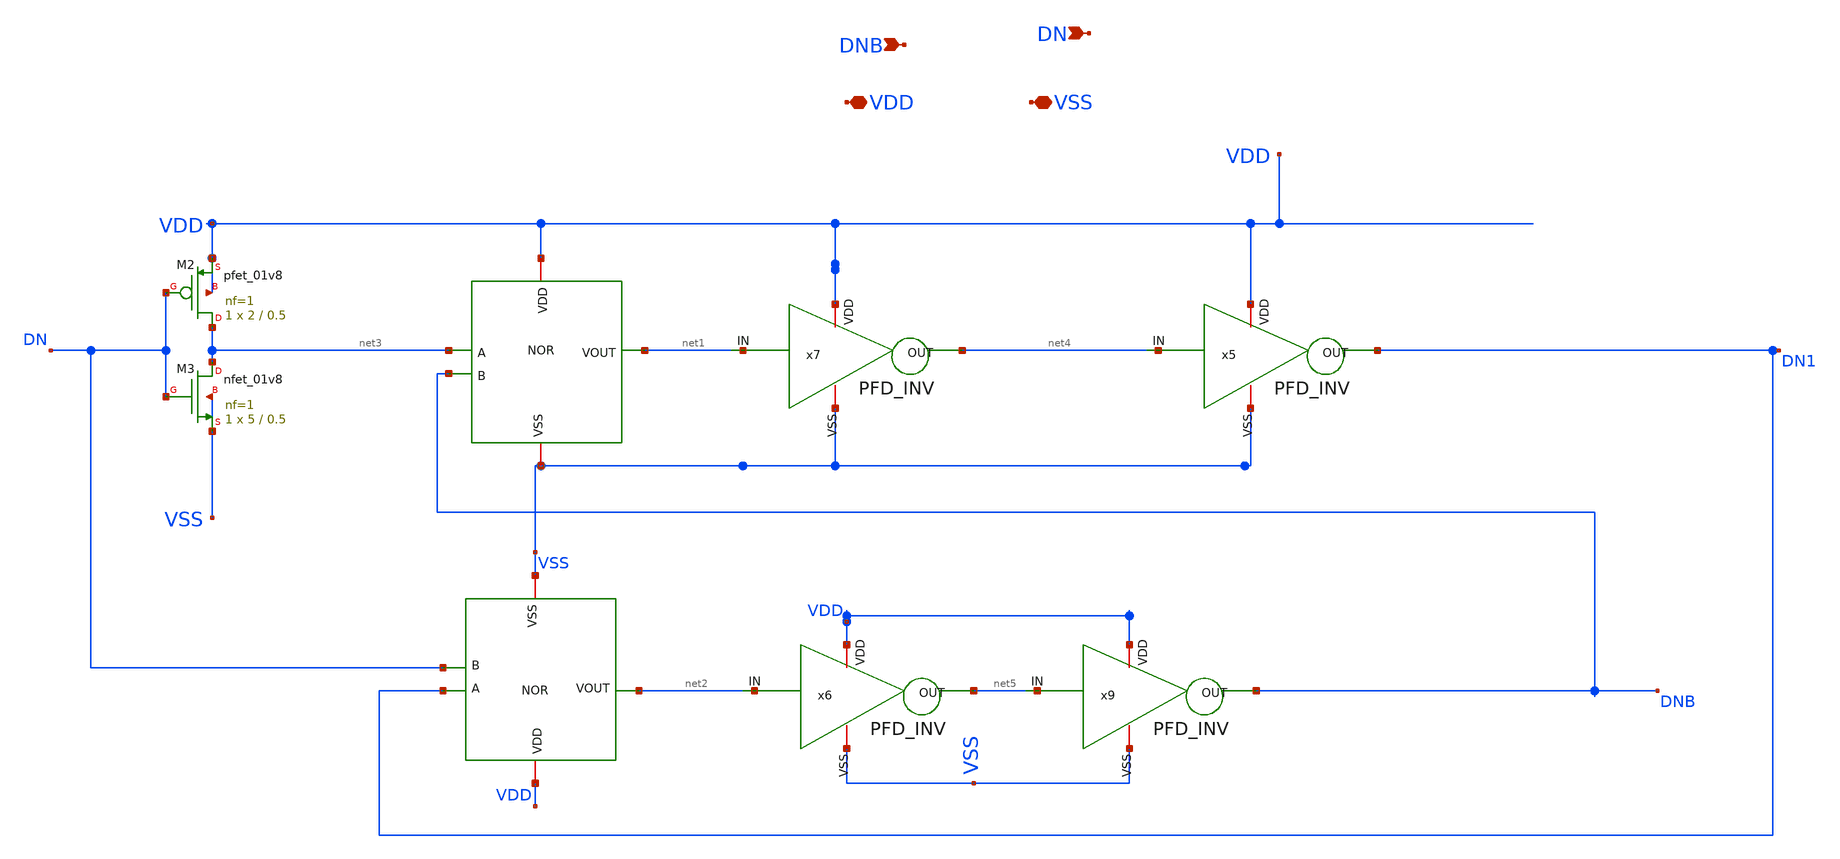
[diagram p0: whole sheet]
** sch_path: Xschem/PLL_TOP_Schematics/untitled.sch
**.subckt untitled DN DNB VDD VSS
*.ipin DN
*.ipin DNB
*.iopin VDD
*.iopin VSS
x3 VDD net3 DNB net1 VSS NOR
x4 VDD DN1 DN net2 VSS NOR
x6 VDD VSS net2 net5 PFD_INV
x7 VDD VSS net1 net4 PFD_INV
XM2 net3 DN VDD VDD sky130_fd_pr__pfet_01v8 L=0.5 W=2 nf=1 ad='int((nf+1)/2) * W/nf * 0.29' as='int((nf+2)/2) * W/nf * 0.29'
+ pd='2*int((nf+1)/2) * (W/nf + 0.29)' ps='2*int((nf+2)/2) * (W/nf + 0.29)' nrd='0.29 / W' nrs='0.29 / W'
+ sa=0 sb=0 sd=0 mult=1 m=1
XM3 net3 DN VSS VSS sky130_fd_pr__nfet_01v8 L=0.5 W=5 nf=1 ad='int((nf+1)/2) * W/nf * 0.29' as='int((nf+2)/2) * W/nf * 0.29'
+ pd='2*int((nf+1)/2) * (W/nf + 0.29)' ps='2*int((nf+2)/2) * (W/nf + 0.29)' nrd='0.29 / W' nrs='0.29 / W'
+ sa=0 sb=0 sd=0 mult=1 m=1
x5 VDD VSS net4 DN1 PFD_INV
x9 VDD VSS net5 DNB PFD_INV
**.ends

* expanding   symbol:  NOR.sym # of pins=5
** sym_path: Xschem/PLL_TOP_Schematics/NOR.sym
** sch_path: Xschem/PLL_TOP_Schematics/NOR.sch
.subckt NOR VDD A B VOUT VSS
*.iopin VSS
*.iopin VDD
*.ipin A
*.ipin B
*.opin VOUT
XM5 VOUT B net1 VDD sky130_fd_pr__pfet_01v8 L=0.2 W=4 nf=1 ad='int((nf+1)/2) * W/nf * 0.29' as='int((nf+2)/2) * W/nf * 0.29'
+ pd='2*int((nf+1)/2) * (W/nf + 0.29)' ps='2*int((nf+2)/2) * (W/nf + 0.29)' nrd='0.29 / W' nrs='0.29 / W'
+ sa=0 sb=0 sd=0 mult=1 m=1
XM1 VOUT A VSS VSS sky130_fd_pr__nfet_01v8 L=0.2 W=1 nf=1 ad='int((nf+1)/2) * W/nf * 0.29' as='int((nf+2)/2) * W/nf * 0.29'
+ pd='2*int((nf+1)/2) * (W/nf + 0.29)' ps='2*int((nf+2)/2) * (W/nf + 0.29)' nrd='0.29 / W' nrs='0.29 / W'
+ sa=0 sb=0 sd=0 mult=1 m=1
XM2 net1 A VDD VDD sky130_fd_pr__pfet_01v8 L=0.2 W=4 nf=1 ad='int((nf+1)/2) * W/nf * 0.29' as='int((nf+2)/2) * W/nf * 0.29'
+ pd='2*int((nf+1)/2) * (W/nf + 0.29)' ps='2*int((nf+2)/2) * (W/nf + 0.29)' nrd='0.29 / W' nrs='0.29 / W'
+ sa=0 sb=0 sd=0 mult=1 m=1
XM3 VOUT B VSS VSS sky130_fd_pr__nfet_01v8 L=0.2 W=1 nf=1 ad='int((nf+1)/2) * W/nf * 0.29' as='int((nf+2)/2) * W/nf * 0.29'
+ pd='2*int((nf+1)/2) * (W/nf + 0.29)' ps='2*int((nf+2)/2) * (W/nf + 0.29)' nrd='0.29 / W' nrs='0.29 / W'
+ sa=0 sb=0 sd=0 mult=1 m=1
.ends


* expanding   symbol:  PFD_INV.sym # of pins=4
** sym_path: Xschem/PLL_TOP_Schematics/PFD_INV.sym
** sch_path: Xschem/PLL_TOP_Schematics/PFD_INV.sch
.subckt PFD_INV VDD VSS IN OUT
*.iopin VDD
*.iopin VSS
*.ipin IN
*.opin OUT
XM1 OUT IN VDD VDD sky130_fd_pr__pfet_01v8 L=0.15 W=0.84 nf=1 ad='int((nf+1)/2) * W/nf * 0.29' as='int((nf+2)/2) * W/nf * 0.29'
+ pd='2*int((nf+1)/2) * (W/nf + 0.29)' ps='2*int((nf+2)/2) * (W/nf + 0.29)' nrd='0.29 / W' nrs='0.29 / W'
+ sa=0 sb=0 sd=0 mult=1 m=1
XM3 OUT IN VSS VSS sky130_fd_pr__nfet_01v8 L=0.15 W=0.42 nf=1 ad='int((nf+1)/2) * W/nf * 0.29' as='int((nf+2)/2) * W/nf * 0.29'
+ pd='2*int((nf+1)/2) * (W/nf + 0.29)' ps='2*int((nf+2)/2) * (W/nf + 0.29)' nrd='0.29 / W' nrs='0.29 / W'
+ sa=0 sb=0 sd=0 mult=1 m=1
.ends

.end
